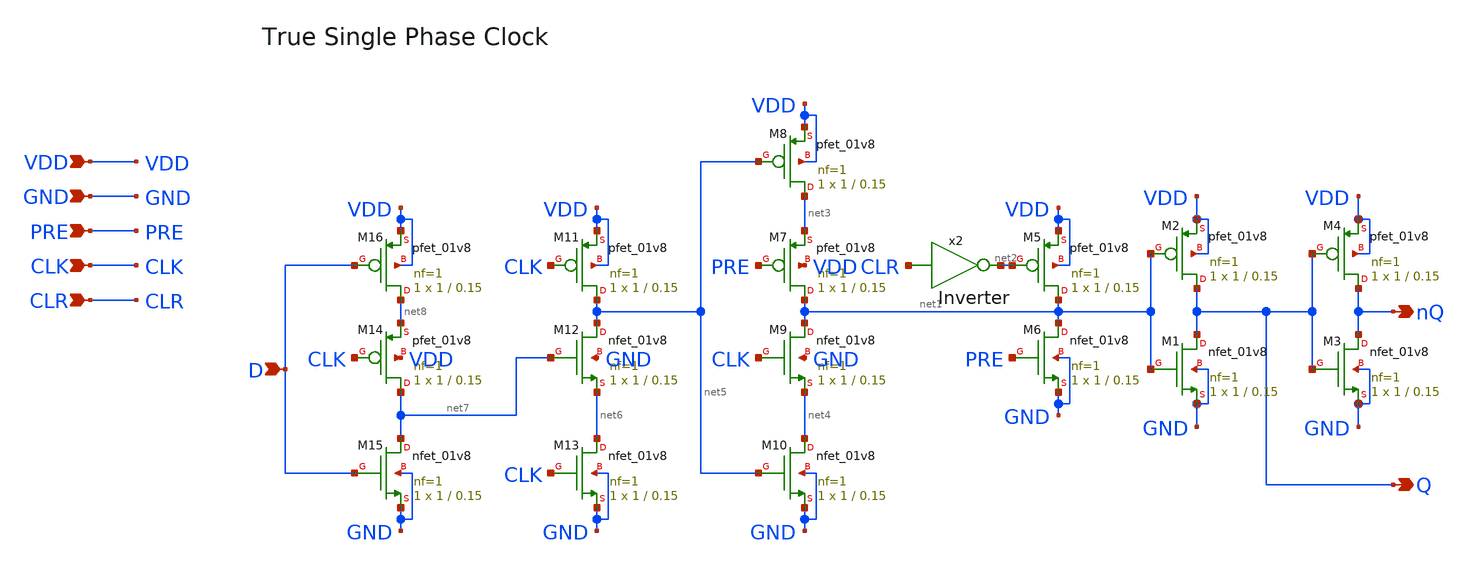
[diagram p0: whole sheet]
** sch_path: xschem/ff.sch
**.subckt ff nQ Q VDD GND D PRE CLR CLK
*.opin nQ
*.opin Q
*.ipin VDD
*.ipin GND
*.ipin D
*.ipin PRE
*.ipin CLR
*.ipin CLK
XM1 Q net1 GND GND sky130_fd_pr__nfet_01v8 L=0.15 W=1 nf=1 ad='int((nf+1)/2) * W/nf * 0.29' as='int((nf+2)/2) * W/nf * 0.29'
+ pd='2*int((nf+1)/2) * (W/nf + 0.29)' ps='2*int((nf+2)/2) * (W/nf + 0.29)' nrd='0.29 / W' nrs='0.29 / W'
+ sa=0 sb=0 sd=0 mult=1 m=1
XM2 Q net1 VDD VDD sky130_fd_pr__pfet_01v8 L=0.15 W=1 nf=1 ad='int((nf+1)/2) * W/nf * 0.29' as='int((nf+2)/2) * W/nf * 0.29'
+ pd='2*int((nf+1)/2) * (W/nf + 0.29)' ps='2*int((nf+2)/2) * (W/nf + 0.29)' nrd='0.29 / W' nrs='0.29 / W'
+ sa=0 sb=0 sd=0 mult=1 m=1
XM3 nQ Q GND GND sky130_fd_pr__nfet_01v8 L=0.15 W=1 nf=1 ad='int((nf+1)/2) * W/nf * 0.29' as='int((nf+2)/2) * W/nf * 0.29'
+ pd='2*int((nf+1)/2) * (W/nf + 0.29)' ps='2*int((nf+2)/2) * (W/nf + 0.29)' nrd='0.29 / W' nrs='0.29 / W'
+ sa=0 sb=0 sd=0 mult=1 m=1
XM4 nQ Q VDD VDD sky130_fd_pr__pfet_01v8 L=0.15 W=1 nf=1 ad='int((nf+1)/2) * W/nf * 0.29' as='int((nf+2)/2) * W/nf * 0.29'
+ pd='2*int((nf+1)/2) * (W/nf + 0.29)' ps='2*int((nf+2)/2) * (W/nf + 0.29)' nrd='0.29 / W' nrs='0.29 / W'
+ sa=0 sb=0 sd=0 mult=1 m=1
XM5 net1 net2 VDD VDD sky130_fd_pr__pfet_01v8 L=0.15 W=1 nf=1 ad='int((nf+1)/2) * W/nf * 0.29' as='int((nf+2)/2) * W/nf * 0.29'
+ pd='2*int((nf+1)/2) * (W/nf + 0.29)' ps='2*int((nf+2)/2) * (W/nf + 0.29)' nrd='0.29 / W' nrs='0.29 / W'
+ sa=0 sb=0 sd=0 mult=1 m=1
XM6 net1 PRE GND GND sky130_fd_pr__nfet_01v8 L=0.15 W=1 nf=1 ad='int((nf+1)/2) * W/nf * 0.29' as='int((nf+2)/2) * W/nf * 0.29'
+ pd='2*int((nf+1)/2) * (W/nf + 0.29)' ps='2*int((nf+2)/2) * (W/nf + 0.29)' nrd='0.29 / W' nrs='0.29 / W'
+ sa=0 sb=0 sd=0 mult=1 m=1
XM7 net1 PRE net3 VDD sky130_fd_pr__pfet_01v8 L=0.15 W=1 nf=1 ad='int((nf+1)/2) * W/nf * 0.29' as='int((nf+2)/2) * W/nf * 0.29'
+ pd='2*int((nf+1)/2) * (W/nf + 0.29)' ps='2*int((nf+2)/2) * (W/nf + 0.29)' nrd='0.29 / W' nrs='0.29 / W'
+ sa=0 sb=0 sd=0 mult=1 m=1
XM8 net3 net5 VDD VDD sky130_fd_pr__pfet_01v8 L=0.15 W=1 nf=1 ad='int((nf+1)/2) * W/nf * 0.29' as='int((nf+2)/2) * W/nf * 0.29'
+ pd='2*int((nf+1)/2) * (W/nf + 0.29)' ps='2*int((nf+2)/2) * (W/nf + 0.29)' nrd='0.29 / W' nrs='0.29 / W'
+ sa=0 sb=0 sd=0 mult=1 m=1
XM9 net1 CLK net4 GND sky130_fd_pr__nfet_01v8 L=0.15 W=1 nf=1 ad='int((nf+1)/2) * W/nf * 0.29' as='int((nf+2)/2) * W/nf * 0.29'
+ pd='2*int((nf+1)/2) * (W/nf + 0.29)' ps='2*int((nf+2)/2) * (W/nf + 0.29)' nrd='0.29 / W' nrs='0.29 / W'
+ sa=0 sb=0 sd=0 mult=1 m=1
XM10 net4 net5 GND GND sky130_fd_pr__nfet_01v8 L=0.15 W=1 nf=1 ad='int((nf+1)/2) * W/nf * 0.29' as='int((nf+2)/2) * W/nf * 0.29'
+ pd='2*int((nf+1)/2) * (W/nf + 0.29)' ps='2*int((nf+2)/2) * (W/nf + 0.29)' nrd='0.29 / W' nrs='0.29 / W'
+ sa=0 sb=0 sd=0 mult=1 m=1
XM11 net5 CLK VDD VDD sky130_fd_pr__pfet_01v8 L=0.15 W=1 nf=1 ad='int((nf+1)/2) * W/nf * 0.29' as='int((nf+2)/2) * W/nf * 0.29'
+ pd='2*int((nf+1)/2) * (W/nf + 0.29)' ps='2*int((nf+2)/2) * (W/nf + 0.29)' nrd='0.29 / W' nrs='0.29 / W'
+ sa=0 sb=0 sd=0 mult=1 m=1
XM12 net5 net7 net6 GND sky130_fd_pr__nfet_01v8 L=0.15 W=1 nf=1 ad='int((nf+1)/2) * W/nf * 0.29' as='int((nf+2)/2) * W/nf * 0.29'
+ pd='2*int((nf+1)/2) * (W/nf + 0.29)' ps='2*int((nf+2)/2) * (W/nf + 0.29)' nrd='0.29 / W' nrs='0.29 / W'
+ sa=0 sb=0 sd=0 mult=1 m=1
XM13 net6 CLK GND GND sky130_fd_pr__nfet_01v8 L=0.15 W=1 nf=1 ad='int((nf+1)/2) * W/nf * 0.29' as='int((nf+2)/2) * W/nf * 0.29'
+ pd='2*int((nf+1)/2) * (W/nf + 0.29)' ps='2*int((nf+2)/2) * (W/nf + 0.29)' nrd='0.29 / W' nrs='0.29 / W'
+ sa=0 sb=0 sd=0 mult=1 m=1
XM15 net7 D GND GND sky130_fd_pr__nfet_01v8 L=0.15 W=1 nf=1 ad='int((nf+1)/2) * W/nf * 0.29' as='int((nf+2)/2) * W/nf * 0.29'
+ pd='2*int((nf+1)/2) * (W/nf + 0.29)' ps='2*int((nf+2)/2) * (W/nf + 0.29)' nrd='0.29 / W' nrs='0.29 / W'
+ sa=0 sb=0 sd=0 mult=1 m=1
XM14 net7 CLK net8 VDD sky130_fd_pr__pfet_01v8 L=0.15 W=1 nf=1 ad='int((nf+1)/2) * W/nf * 0.29' as='int((nf+2)/2) * W/nf * 0.29'
+ pd='2*int((nf+1)/2) * (W/nf + 0.29)' ps='2*int((nf+2)/2) * (W/nf + 0.29)' nrd='0.29 / W' nrs='0.29 / W'
+ sa=0 sb=0 sd=0 mult=1 m=1
XM16 net8 D VDD VDD sky130_fd_pr__pfet_01v8 L=0.15 W=1 nf=1 ad='int((nf+1)/2) * W/nf * 0.29' as='int((nf+2)/2) * W/nf * 0.29'
+ pd='2*int((nf+1)/2) * (W/nf + 0.29)' ps='2*int((nf+2)/2) * (W/nf + 0.29)' nrd='0.29 / W' nrs='0.29 / W'
+ sa=0 sb=0 sd=0 mult=1 m=1
x2 net2 CLR Inverter
**.ends

* expanding   symbol:  Inverter.sym # of pins=2
** sym_path: xschem/Inverter.sym
** sch_path: xschem/Inverter.sch
.subckt Inverter Vout Vin
*.ipin Vin
*.opin Vout
XM1 Vout Vin GND GND sky130_fd_pr__nfet_01v8 L=0.15 W=1 nf=1 ad='int((nf+1)/2) * W/nf * 0.29' as='int((nf+2)/2) * W/nf * 0.29'
+ pd='2*int((nf+1)/2) * (W/nf + 0.29)' ps='2*int((nf+2)/2) * (W/nf + 0.29)' nrd='0.29 / W' nrs='0.29 / W'
+ sa=0 sb=0 sd=0 mult=1 m=1
XM2 Vout Vin VDD VDD sky130_fd_pr__pfet_01v8 L=0.15 W=4 nf=1 ad='int((nf+1)/2) * W/nf * 0.29' as='int((nf+2)/2) * W/nf * 0.29'
+ pd='2*int((nf+1)/2) * (W/nf + 0.29)' ps='2*int((nf+2)/2) * (W/nf + 0.29)' nrd='0.29 / W' nrs='0.29 / W'
+ sa=0 sb=0 sd=0 mult=1 m=1
V1 VDD GND 1.8
.ends

.GLOBAL GND
.end
